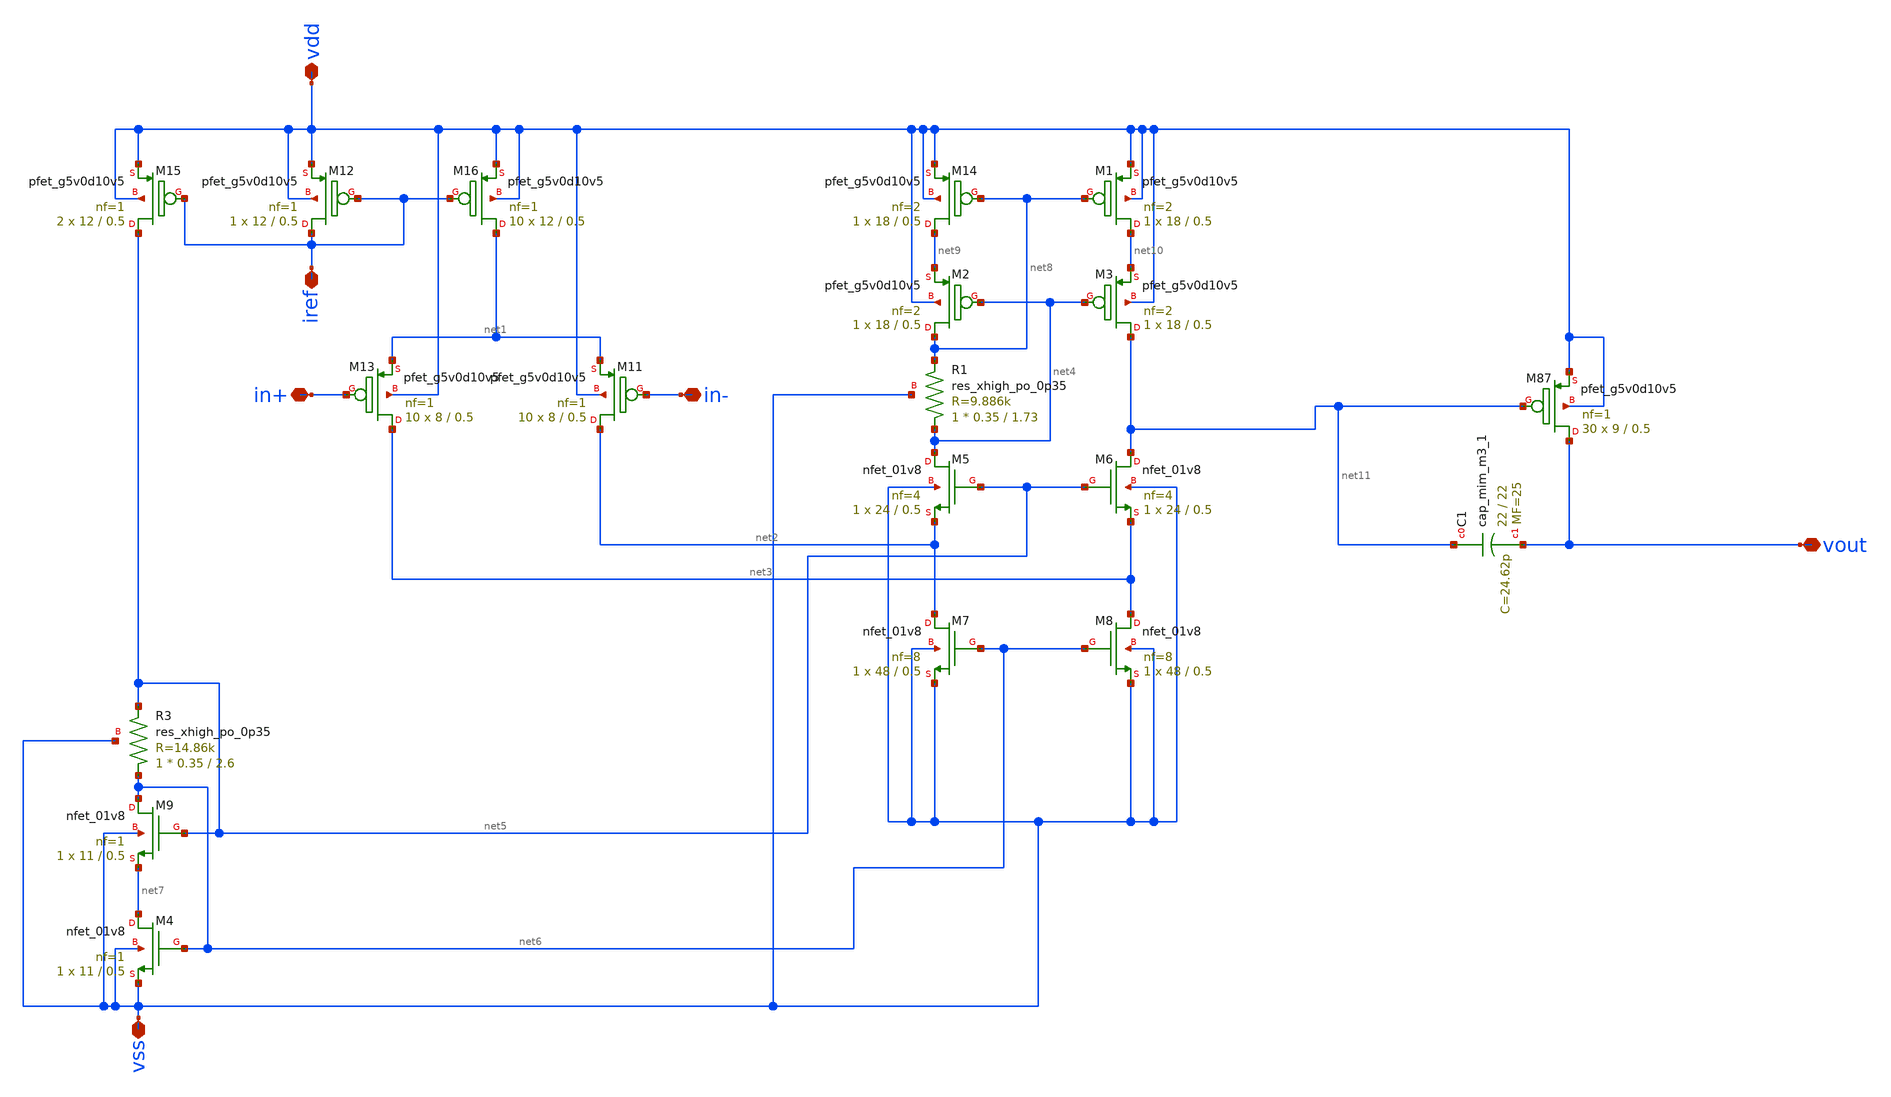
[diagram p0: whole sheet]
** sch_path: analog/analog_ldo/ceyda_src/ldos_wores.sch
**.subckt ldos_wores vss iref vdd in+ vout in-
*.iopin vss
*.iopin iref
*.iopin vdd
*.iopin in+
*.iopin vout
*.iopin in-
XM9 net6 net5 net7 vss sky130_fd_pr__nfet_01v8 L=0.5 W=11 nf=1 ad='int((nf+1)/2) * W/nf * 0.29' as='int((nf+2)/2) * W/nf * 0.29'
+ pd='2*int((nf+1)/2) * (W/nf + 0.29)' ps='2*int((nf+2)/2) * (W/nf + 0.29)' nrd='0.29 / W' nrs='0.29 / W'
+ sa=0 sb=0 sd=0 mult=1 m=1
XM4 net7 net6 vss vss sky130_fd_pr__nfet_01v8 L=0.5 W=11 nf=1 ad='int((nf+1)/2) * W/nf * 0.29' as='int((nf+2)/2) * W/nf * 0.29'
+ pd='2*int((nf+1)/2) * (W/nf + 0.29)' ps='2*int((nf+2)/2) * (W/nf + 0.29)' nrd='0.29 / W' nrs='0.29 / W'
+ sa=0 sb=0 sd=0 mult=1 m=1
XM5 net4 net5 net2 vss sky130_fd_pr__nfet_01v8 L=0.5 W=24 nf=4 ad='int((nf+1)/2) * W/nf * 0.29' as='int((nf+2)/2) * W/nf * 0.29'
+ pd='2*int((nf+1)/2) * (W/nf + 0.29)' ps='2*int((nf+2)/2) * (W/nf + 0.29)' nrd='0.29 / W' nrs='0.29 / W'
+ sa=0 sb=0 sd=0 mult=1 m=1
XM6 net11 net5 net3 vss sky130_fd_pr__nfet_01v8 L=0.5 W=24 nf=4 ad='int((nf+1)/2) * W/nf * 0.29' as='int((nf+2)/2) * W/nf * 0.29'
+ pd='2*int((nf+1)/2) * (W/nf + 0.29)' ps='2*int((nf+2)/2) * (W/nf + 0.29)' nrd='0.29 / W' nrs='0.29 / W'
+ sa=0 sb=0 sd=0 mult=1 m=1
XM7 net2 net6 vss vss sky130_fd_pr__nfet_01v8 L=0.5 W=48 nf=8 ad='int((nf+1)/2) * W/nf * 0.29' as='int((nf+2)/2) * W/nf * 0.29'
+ pd='2*int((nf+1)/2) * (W/nf + 0.29)' ps='2*int((nf+2)/2) * (W/nf + 0.29)' nrd='0.29 / W' nrs='0.29 / W'
+ sa=0 sb=0 sd=0 mult=1 m=1
XM8 net3 net6 vss vss sky130_fd_pr__nfet_01v8 L=0.5 W=48 nf=8 ad='int((nf+1)/2) * W/nf * 0.29' as='int((nf+2)/2) * W/nf * 0.29'
+ pd='2*int((nf+1)/2) * (W/nf + 0.29)' ps='2*int((nf+2)/2) * (W/nf + 0.29)' nrd='0.29 / W' nrs='0.29 / W'
+ sa=0 sb=0 sd=0 mult=1 m=1
XM15 net5 iref vdd vdd sky130_fd_pr__pfet_g5v0d10v5 L=0.5 W=12 nf=1 ad='int((nf+1)/2) * W/nf * 0.29'
+ as='int((nf+2)/2) * W/nf * 0.29' pd='2*int((nf+1)/2) * (W/nf + 0.29)' ps='2*int((nf+2)/2) * (W/nf + 0.29)'
+ nrd='0.29 / W' nrs='0.29 / W' sa=0 sb=0 sd=0 mult=2 m=2
XM12 iref iref vdd vdd sky130_fd_pr__pfet_g5v0d10v5 L=0.5 W=12 nf=1 ad='int((nf+1)/2) * W/nf * 0.29'
+ as='int((nf+2)/2) * W/nf * 0.29' pd='2*int((nf+1)/2) * (W/nf + 0.29)' ps='2*int((nf+2)/2) * (W/nf + 0.29)'
+ nrd='0.29 / W' nrs='0.29 / W' sa=0 sb=0 sd=0 mult=1 m=1
XM16 net1 iref vdd vdd sky130_fd_pr__pfet_g5v0d10v5 L=0.5 W=12 nf=1 ad='int((nf+1)/2) * W/nf * 0.29'
+ as='int((nf+2)/2) * W/nf * 0.29' pd='2*int((nf+1)/2) * (W/nf + 0.29)' ps='2*int((nf+2)/2) * (W/nf + 0.29)'
+ nrd='0.29 / W' nrs='0.29 / W' sa=0 sb=0 sd=0 mult=10 m=10
XM13 net3 in+ net1 vdd sky130_fd_pr__pfet_g5v0d10v5 L=0.5 W=8 nf=1 ad='int((nf+1)/2) * W/nf * 0.29' as='int((nf+2)/2) * W/nf * 0.29'
+ pd='2*int((nf+1)/2) * (W/nf + 0.29)' ps='2*int((nf+2)/2) * (W/nf + 0.29)' nrd='0.29 / W' nrs='0.29 / W'
+ sa=0 sb=0 sd=0 mult=10 m=10
XM11 net2 in- net1 vdd sky130_fd_pr__pfet_g5v0d10v5 L=0.5 W=8 nf=1 ad='int((nf+1)/2) * W/nf * 0.29' as='int((nf+2)/2) * W/nf * 0.29'
+ pd='2*int((nf+1)/2) * (W/nf + 0.29)' ps='2*int((nf+2)/2) * (W/nf + 0.29)' nrd='0.29 / W' nrs='0.29 / W'
+ sa=0 sb=0 sd=0 mult=10 m=10
XM14 net9 net8 vdd vdd sky130_fd_pr__pfet_g5v0d10v5 L=0.5 W=18 nf=2 ad='int((nf+1)/2) * W/nf * 0.29'
+ as='int((nf+2)/2) * W/nf * 0.29' pd='2*int((nf+1)/2) * (W/nf + 0.29)' ps='2*int((nf+2)/2) * (W/nf + 0.29)'
+ nrd='0.29 / W' nrs='0.29 / W' sa=0 sb=0 sd=0 mult=1 m=1
XM2 net8 net4 net9 vdd sky130_fd_pr__pfet_g5v0d10v5 L=0.5 W=18 nf=2 ad='int((nf+1)/2) * W/nf * 0.29'
+ as='int((nf+2)/2) * W/nf * 0.29' pd='2*int((nf+1)/2) * (W/nf + 0.29)' ps='2*int((nf+2)/2) * (W/nf + 0.29)'
+ nrd='0.29 / W' nrs='0.29 / W' sa=0 sb=0 sd=0 mult=1 m=1
XM1 net10 net8 vdd vdd sky130_fd_pr__pfet_g5v0d10v5 L=0.5 W=18 nf=2 ad='int((nf+1)/2) * W/nf * 0.29'
+ as='int((nf+2)/2) * W/nf * 0.29' pd='2*int((nf+1)/2) * (W/nf + 0.29)' ps='2*int((nf+2)/2) * (W/nf + 0.29)'
+ nrd='0.29 / W' nrs='0.29 / W' sa=0 sb=0 sd=0 mult=1 m=1
XM3 net11 net4 net10 vdd sky130_fd_pr__pfet_g5v0d10v5 L=0.5 W=18 nf=2 ad='int((nf+1)/2) * W/nf * 0.29'
+ as='int((nf+2)/2) * W/nf * 0.29' pd='2*int((nf+1)/2) * (W/nf + 0.29)' ps='2*int((nf+2)/2) * (W/nf + 0.29)'
+ nrd='0.29 / W' nrs='0.29 / W' sa=0 sb=0 sd=0 mult=1 m=1
XR3 net6 net5 vss sky130_fd_pr__res_xhigh_po_0p35 L=2.6 mult=1 m=1
XR1 net4 net8 vss sky130_fd_pr__res_xhigh_po_0p35 L=1.73 mult=1 m=1
XM87 vout net11 vdd vdd sky130_fd_pr__pfet_g5v0d10v5 L=0.5 W=9 nf=1 ad='int((nf+1)/2) * W/nf * 0.29'
+ as='int((nf+2)/2) * W/nf * 0.29' pd='2*int((nf+1)/2) * (W/nf + 0.29)' ps='2*int((nf+2)/2) * (W/nf + 0.29)'
+ nrd='0.29 / W' nrs='0.29 / W' sa=0 sb=0 sd=0 mult=30 m=30
XC1 net11 vout sky130_fd_pr__cap_mim_m3_1 W=22 L=22 MF=25 m=25
**** begin user architecture code

** opencircuitdesign pdks install
.lib $::SKYWATER_MODELS/sky130.lib.spice tt


**** end user architecture code
**.ends
.end
